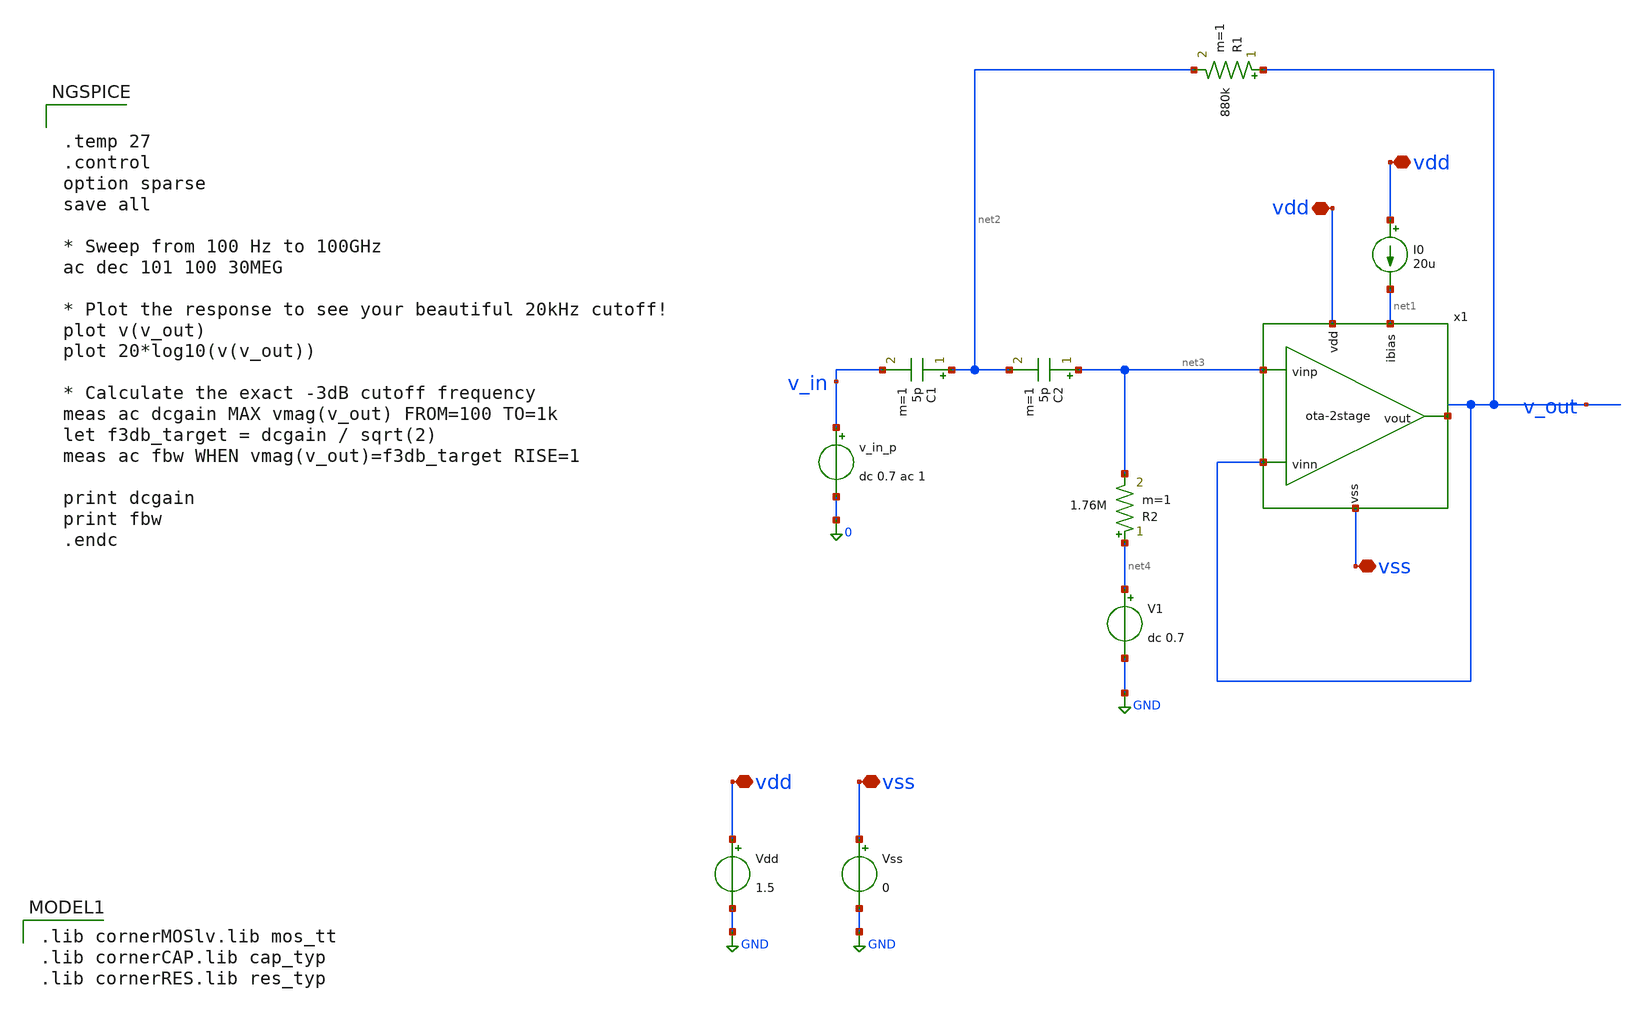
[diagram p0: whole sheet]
** sch_path: Testbench/ota-2stage_tb-sk-hpf.sch
**.subckt ota-2stage_tb-sk-hpf vdd vdd vdd vss vss
*.iopin vdd
*.iopin vdd
*.iopin vdd
*.iopin vss
*.iopin vss
I0 vdd net1 20u
Vdd vdd GND 1.5
Vss vss GND 0
v_in_p v_in 0 dc 0.7 ac 1
x1 vdd net1 v_out net5 net3 vss ota-2stage
R1 v_out net2 880k m=1
R2 net4 net3 1.76M m=1
C1 net2 v_in 5p m=1
C2 net3 net2 5p m=1
V1 net4 GND dc 0.7
**** begin user architecture code


.temp 27
.control
option sparse
save all

* Sweep from 100 Hz to 100GHz
ac dec 101 100 30MEG

* Plot the response to see your beautiful 20kHz cutoff!
plot v(v_out)
plot 20*log10(v(v_out))

* Calculate the exact -3dB cutoff frequency
meas ac dcgain MAX vmag(v_out) FROM=100 TO=1k
let f3db_target = dcgain / sqrt(2)
meas ac fbw WHEN vmag(v_out)=f3db_target RISE=1

print dcgain
print fbw
.endc


 .lib cornerMOSlv.lib mos_tt
.lib cornerCAP.lib cap_typ
.lib cornerRES.lib res_typ

**** end user architecture code
**.ends

* expanding   symbol:  ota-2stage.sym # of pins=6
** sym_path: Testbench/ota-2stage.sym
** sch_path: Testbench/ota-2stage.sch
.subckt ota-2stage vdd ibias vinn vout vinp vss
*.iopin vdd
*.iopin vss
*.ipin ibias
*.ipin vout
*.ipin vinn
*.ipin vinp
XM1 net1 vinn net3 net3 sg13_lv_nmos w=2u l=5u ng=1 m=1 mm_ok=1
XM2 net2 vinp net3 net3 sg13_lv_nmos w=2u l=5u ng=1 m=1 mm_ok=1
XM4 net2 net1 vdd vdd sg13_lv_pmos w=2.5u l=5u ng=1 m=1 mm_ok=1
XM3 net1 net1 vdd vdd sg13_lv_pmos w=2.5u l=5u ng=1 m=1 mm_ok=1
XM5 vout net2 vdd vdd sg13_lv_pmos w=6.25u l=5u ng=5 m=1 mm_ok=1
XM6 ibias ibias vss vss sg13_lv_nmos w=5u l=5u ng=1 m=1 mm_ok=1
XM7 net3 ibias vss vss sg13_lv_nmos w=1u l=5u ng=1 m=1 mm_ok=1
XM8 vout ibias vss vss sg13_lv_nmos w=6.25u l=5u ng=1 m=1 mm_ok=1
XCM net2 vout cap_cmim w=14.2e-6 l=14.2e-6 m=1 mm_ok=1
.ends

.GLOBAL GND
.end
